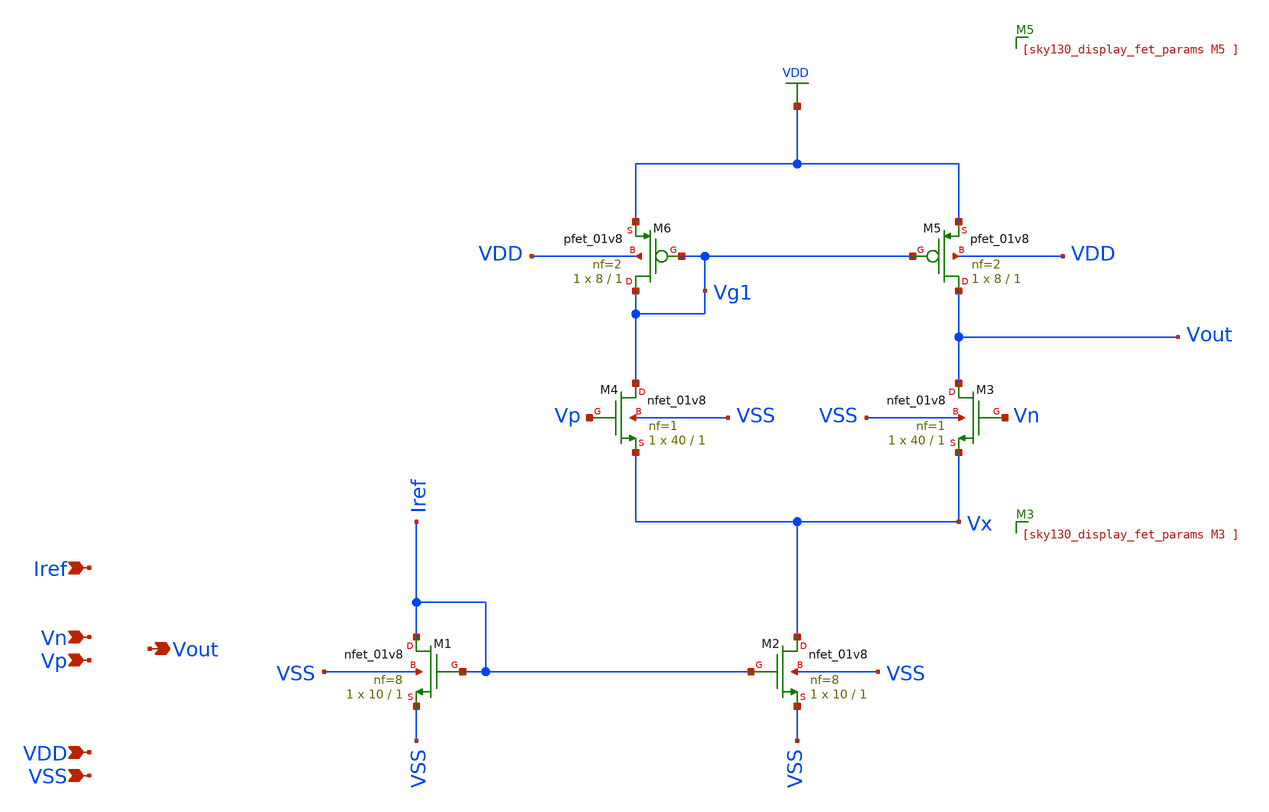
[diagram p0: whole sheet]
** sch_path: xschem/opamp.sch
**.subckt opamp VSS Vp Vout Vn VDD Iref
*.ipin VSS
*.ipin Vp
*.opin Vout
*.ipin Vn
*.ipin VDD
*.ipin Iref
XM1 Iref Iref VSS VSS sky130_fd_pr__nfet_01v8 L=1 W=10 nf=8 ad='int((8 + 1)/2) * 10 / 8 * 0.29' as='int((8 + 2)/2) * 10 / 8 * 0.29'
+ pd='2*int((8 + 1)/2) * (10 / 8 + 0.29)' ps='2*int((8 + 2)/2) * (10 / 8 + 0.29)' nrd='0.29 / 10 ' nrs='0.29 / 10 '
+ sa=0 sb=0 sd=0 mult=1 m=1
XM2 Vx Iref VSS VSS sky130_fd_pr__nfet_01v8 L=1 W=10 nf=8 ad='int((8 + 1)/2) * 10 / 8 * 0.29' as='int((8 + 2)/2) * 10 / 8 * 0.29'
+ pd='2*int((8 + 1)/2) * (10 / 8 + 0.29)' ps='2*int((8 + 2)/2) * (10 / 8 + 0.29)' nrd='0.29 / 10 ' nrs='0.29 / 10 '
+ sa=0 sb=0 sd=0 mult=1 m=1
XM3 Vout Vn Vx VSS sky130_fd_pr__nfet_01v8 L=1 W=40 nf=1 ad='int((1 + 1)/2) * 40 / 1 * 0.29' as='int((1 + 2)/2) * 40 / 1 * 0.29'
+ pd='2*int((1 + 1)/2) * (40 / 1 + 0.29)' ps='2*int((1 + 2)/2) * (40 / 1 + 0.29)' nrd='0.29 / 40 ' nrs='0.29 / 40 '
+ sa=0 sb=0 sd=0 mult=1 m=1
XM4 Vg1 Vp Vx VSS sky130_fd_pr__nfet_01v8 L=1 W=40 nf=1 ad='int((1 + 1)/2) * 40 / 1 * 0.29' as='int((1 + 2)/2) * 40 / 1 * 0.29'
+ pd='2*int((1 + 1)/2) * (40 / 1 + 0.29)' ps='2*int((1 + 2)/2) * (40 / 1 + 0.29)' nrd='0.29 / 40 ' nrs='0.29 / 40 '
+ sa=0 sb=0 sd=0 mult=1 m=1
XM5 Vout Vg1 VDD VDD sky130_fd_pr__pfet_01v8 L=1 W=8 nf=2 ad='int((2 + 1)/2) * 8 / 2 * 0.29' as='int((2 + 2)/2) * 8 / 2 * 0.29'
+ pd='2*int((2 + 1)/2) * (8 / 2 + 0.29)' ps='2*int((2 + 2)/2) * (8 / 2 + 0.29)' nrd='0.29 / 8 ' nrs='0.29 / 8 '
+ sa=0 sb=0 sd=0 mult=1 m=1
XM6 Vg1 Vg1 VDD VDD sky130_fd_pr__pfet_01v8 L=1 W=8 nf=2 ad='int((2 + 1)/2) * 8 / 2 * 0.29' as='int((2 + 2)/2) * 8 / 2 * 0.29'
+ pd='2*int((2 + 1)/2) * (8 / 2 + 0.29)' ps='2*int((2 + 2)/2) * (8 / 2 + 0.29)' nrd='0.29 / 8 ' nrs='0.29 / 8 '
+ sa=0 sb=0 sd=0 mult=1 m=1
**.ends
.GLOBAL VDD
.end
